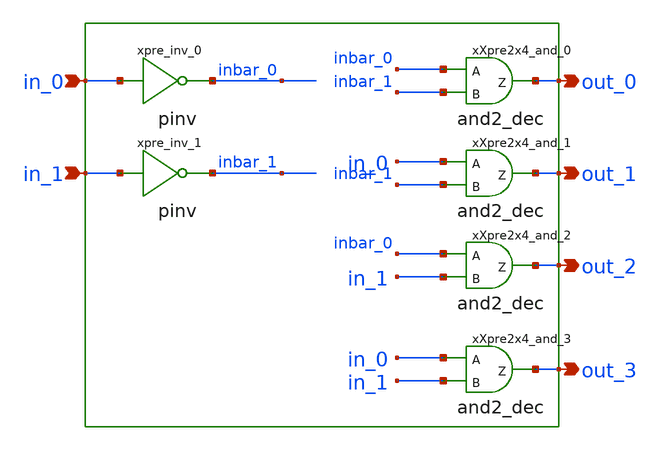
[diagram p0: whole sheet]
** sch_path: sram_4_16_scn4m/hierarchical_predecode2x4.sch
**.subckt hierarchical_predecode2x4 in_0 in_1 out_0 out_1 out_2 out_3
*.ipin in_0
*.ipin in_1
*.opin out_0
*.opin out_1
*.opin out_2
*.opin out_3
xpre_inv_0 in_0 inbar_0 vdd gnd pinv
xpre_inv_1 in_1 inbar_1 vdd gnd pinv
xXpre2x4_and_0 inbar_0 inbar_1 out_0 and2_dec
xXpre2x4_and_1 in_0 inbar_1 out_1 and2_dec
xXpre2x4_and_2 inbar_0 in_1 out_2 and2_dec
xXpre2x4_and_3 in_0 in_1 out_3 and2_dec
**.ends

* expanding   symbol:  pinv.sym # of pins=2
** sym_path: sram_4_16_scn4m/pinv.sym
** sch_path: sram_4_16_scn4m/pinv.sch
.subckt pinv A Z vdd gnd
*.ipin A
*.opin Z
XMpinv_nmos Z A gnd gnd sky130_fd_pr__nfet_01v8 L=0.4 W=0.8 nf=1 ad='int((nf+1)/2) * W/nf * 0.29' as='int((nf+2)/2) * W/nf * 0.29'
+ pd='2*int((nf+1)/2) * (W/nf + 0.29)' ps='2*int((nf+2)/2) * (W/nf + 0.29)' nrd='0.29 / W' nrs='0.29 / W'
+ sa=0 sb=0 sd=0 mult=1 m=1
XMp_inv_pmos Z A vdd vdd sky130_fd_pr__pfet_01v8 L=0.4 W=1.6 nf=1 ad='int((nf+1)/2) * W/nf * 0.29' as='int((nf+2)/2) * W/nf * 0.29'
+ pd='2*int((nf+1)/2) * (W/nf + 0.29)' ps='2*int((nf+2)/2) * (W/nf + 0.29)' nrd='0.29 / W' nrs='0.29 / W'
+ sa=0 sb=0 sd=0 mult=1 m=1
.ends


* expanding   symbol:  and2_dec.sym # of pins=3
** sym_path: sram_4_16_scn4m/and2_dec.sym
** sch_path: sram_4_16_scn4m/and2_dec.sch
.subckt and2_dec A B Z
*.ipin A
*.ipin B
*.opin Z
xpand2_dec_nand A B zb_int vdd gnd pnand2
xpand2_dec_inv zb_int Z vdd gnd pinv
.ends


* expanding   symbol:  pnand2.sym # of pins=3
** sym_path: sram_2_64_scn4m/pnand2.sym
** sch_path: sram_2_64_scn4m/pnand2.sch
.subckt pnand2 A B Z vdd gnd
*.ipin A
*.ipin B
*.opin Z
*.iopin vdd
*.iopin gnd
XMpnand2_nmos1 Z B net1 gnd sky130_fd_pr__nfet_01v8 L=0.4 W=1.6 nf=1 ad='int((nf+1)/2) * W/nf * 0.29'
+ as='int((nf+2)/2) * W/nf * 0.29' pd='2*int((nf+1)/2) * (W/nf + 0.29)' ps='2*int((nf+2)/2) * (W/nf + 0.29)'
+ nrd='0.29 / W' nrs='0.29 / W' sa=0 sb=0 sd=0 mult=1 m=1
XMpnand2_pmos1 Z A vdd vdd sky130_fd_pr__pfet_01v8 L=0.4 W=1.6 nf=1 ad='int((nf+1)/2) * W/nf * 0.29'
+ as='int((nf+2)/2) * W/nf * 0.29' pd='2*int((nf+1)/2) * (W/nf + 0.29)' ps='2*int((nf+2)/2) * (W/nf + 0.29)'
+ nrd='0.29 / W' nrs='0.29 / W' sa=0 sb=0 sd=0 mult=1 m=1
XMpnand2_pmos2 Z B vdd vdd sky130_fd_pr__pfet_01v8 L=0.4 W=1.6 nf=1 ad='int((nf+1)/2) * W/nf * 0.29'
+ as='int((nf+2)/2) * W/nf * 0.29' pd='2*int((nf+1)/2) * (W/nf + 0.29)' ps='2*int((nf+2)/2) * (W/nf + 0.29)'
+ nrd='0.29 / W' nrs='0.29 / W' sa=0 sb=0 sd=0 mult=1 m=1
XMpnand2_nmos2 net1 A gnd gnd sky130_fd_pr__nfet_01v8 L=0.4 W=1.6 nf=1 ad='int((nf+1)/2) * W/nf * 0.29'
+ as='int((nf+2)/2) * W/nf * 0.29' pd='2*int((nf+1)/2) * (W/nf + 0.29)' ps='2*int((nf+2)/2) * (W/nf + 0.29)'
+ nrd='0.29 / W' nrs='0.29 / W' sa=0 sb=0 sd=0 mult=1 m=1
.ends

.end
